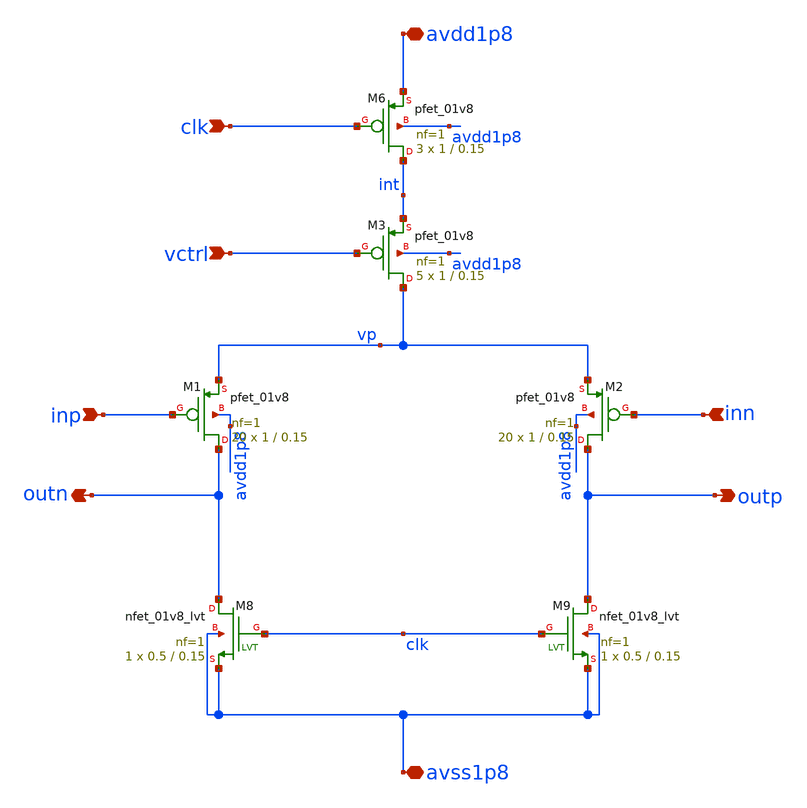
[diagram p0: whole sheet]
** sch_path: xschem/res_amp_lin.sch
**.subckt res_amp_lin avdd1p8 avss1p8 outp outn inn inp clk vctrl
*.iopin avdd1p8
*.iopin avss1p8
*.opin outp
*.opin outn
*.ipin inn
*.ipin inp
*.ipin clk
*.ipin vctrl
XM6 int clk avdd1p8 avdd1p8 sky130_fd_pr__pfet_01v8 L=0.15 W=1 nf=1 ad='int((nf+1)/2) * W/nf * 0.29'
+ as='int((nf+2)/2) * W/nf * 0.29' pd='2*int((nf+1)/2) * (W/nf + 0.29)' ps='2*int((nf+2)/2) * (W/nf + 0.29)'
+ nrd='0.29 / W' nrs='0.29 / W' sa=0 sb=0 sd=0 mult=3 m=3
XM8 outn clk avss1p8 avss1p8 sky130_fd_pr__nfet_01v8_lvt L=0.15 W=0.5 nf=1 ad='int((nf+1)/2) * W/nf * 0.29'
+ as='int((nf+2)/2) * W/nf * 0.29' pd='2*int((nf+1)/2) * (W/nf + 0.29)' ps='2*int((nf+2)/2) * (W/nf + 0.29)'
+ nrd='0.29 / W' nrs='0.29 / W' sa=0 sb=0 sd=0 mult=1 m=1
XM9 outp clk avss1p8 avss1p8 sky130_fd_pr__nfet_01v8_lvt L=0.15 W=0.5 nf=1 ad='int((nf+1)/2) * W/nf * 0.29'
+ as='int((nf+2)/2) * W/nf * 0.29' pd='2*int((nf+1)/2) * (W/nf + 0.29)' ps='2*int((nf+2)/2) * (W/nf + 0.29)'
+ nrd='0.29 / W' nrs='0.29 / W' sa=0 sb=0 sd=0 mult=1 m=1
XM3 vp vctrl int avdd1p8 sky130_fd_pr__pfet_01v8 L=0.15 W=1 nf=1 ad='int((nf+1)/2) * W/nf * 0.29' as='int((nf+2)/2) * W/nf * 0.29'
+ pd='2*int((nf+1)/2) * (W/nf + 0.29)' ps='2*int((nf+2)/2) * (W/nf + 0.29)' nrd='0.29 / W' nrs='0.29 / W'
+ sa=0 sb=0 sd=0 mult=5 m=5
XM1 outn inp vp avdd1p8 sky130_fd_pr__pfet_01v8 L=0.15 W=1 nf=1 ad='int((nf+1)/2) * W/nf * 0.29' as='int((nf+2)/2) * W/nf * 0.29'
+ pd='2*int((nf+1)/2) * (W/nf + 0.29)' ps='2*int((nf+2)/2) * (W/nf + 0.29)' nrd='0.29 / W' nrs='0.29 / W'
+ sa=0 sb=0 sd=0 mult=20 m=20
XM2 outp inn vp avdd1p8 sky130_fd_pr__pfet_01v8 L=0.15 W=1 nf=1 ad='int((nf+1)/2) * W/nf * 0.29' as='int((nf+2)/2) * W/nf * 0.29'
+ pd='2*int((nf+1)/2) * (W/nf + 0.29)' ps='2*int((nf+2)/2) * (W/nf + 0.29)' nrd='0.29 / W' nrs='0.29 / W'
+ sa=0 sb=0 sd=0 mult=20 m=20
**.ends
.end
